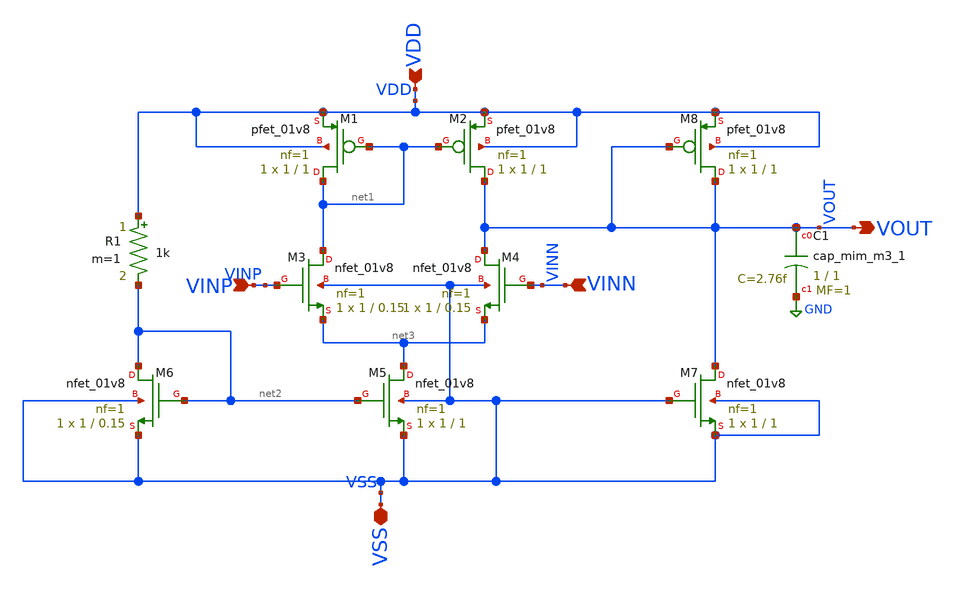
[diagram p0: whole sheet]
** sch_path: schematics/opamp_single_stage.sch
**.subckt opamp_single_stage VSS VOUT VDD VINP VINN
*.iopin VSS
*.opin VOUT
*.ipin VDD
*.ipin VINP
*.ipin VINN
XM1 net1 net1 VDD VDD sky130_fd_pr__pfet_01v8 L=1 W=1 nf=1 ad='int((nf+1)/2) * W/nf * 0.29' as='int((nf+2)/2) * W/nf * 0.29'
+ pd='2*int((nf+1)/2) * (W/nf + 0.29)' ps='2*int((nf+2)/2) * (W/nf + 0.29)' nrd='0.29 / W' nrs='0.29 / W'
+ sa=0 sb=0 sd=0 mult=1 m=1
XM2 VOUT net1 VDD VDD sky130_fd_pr__pfet_01v8 L=1 W=1 nf=1 ad='int((nf+1)/2) * W/nf * 0.29' as='int((nf+2)/2) * W/nf * 0.29'
+ pd='2*int((nf+1)/2) * (W/nf + 0.29)' ps='2*int((nf+2)/2) * (W/nf + 0.29)' nrd='0.29 / W' nrs='0.29 / W'
+ sa=0 sb=0 sd=0 mult=1 m=1
XM3 net1 VINP net3 VSS sky130_fd_pr__nfet_01v8 L=0.15 W=1 nf=1 ad='int((nf+1)/2) * W/nf * 0.29' as='int((nf+2)/2) * W/nf * 0.29'
+ pd='2*int((nf+1)/2) * (W/nf + 0.29)' ps='2*int((nf+2)/2) * (W/nf + 0.29)' nrd='0.29 / W' nrs='0.29 / W'
+ sa=0 sb=0 sd=0 mult=1 m=1
XM4 VOUT VINN net3 VSS sky130_fd_pr__nfet_01v8 L=0.15 W=1 nf=1 ad='int((nf+1)/2) * W/nf * 0.29' as='int((nf+2)/2) * W/nf * 0.29'
+ pd='2*int((nf+1)/2) * (W/nf + 0.29)' ps='2*int((nf+2)/2) * (W/nf + 0.29)' nrd='0.29 / W' nrs='0.29 / W'
+ sa=0 sb=0 sd=0 mult=1 m=1
XM5 net3 net2 VSS VSS sky130_fd_pr__nfet_01v8 L=1 W=1 nf=1 ad='int((nf+1)/2) * W/nf * 0.29' as='int((nf+2)/2) * W/nf * 0.29'
+ pd='2*int((nf+1)/2) * (W/nf + 0.29)' ps='2*int((nf+2)/2) * (W/nf + 0.29)' nrd='0.29 / W' nrs='0.29 / W'
+ sa=0 sb=0 sd=0 mult=1 m=1
XM6 net2 net2 VSS VSS sky130_fd_pr__nfet_01v8 L=0.15 W=1 nf=1 ad='int((nf+1)/2) * W/nf * 0.29' as='int((nf+2)/2) * W/nf * 0.29'
+ pd='2*int((nf+1)/2) * (W/nf + 0.29)' ps='2*int((nf+2)/2) * (W/nf + 0.29)' nrd='0.29 / W' nrs='0.29 / W'
+ sa=0 sb=0 sd=0 mult=1 m=1
XM7 VOUT VSS VSS VSS sky130_fd_pr__nfet_01v8 L=1 W=1 nf=1 ad='int((nf+1)/2) * W/nf * 0.29' as='int((nf+2)/2) * W/nf * 0.29'
+ pd='2*int((nf+1)/2) * (W/nf + 0.29)' ps='2*int((nf+2)/2) * (W/nf + 0.29)' nrd='0.29 / W' nrs='0.29 / W'
+ sa=0 sb=0 sd=0 mult=1 m=1
XM8 VOUT VOUT VDD VDD sky130_fd_pr__pfet_01v8 L=1 W=1 nf=1 ad='int((nf+1)/2) * W/nf * 0.29' as='int((nf+2)/2) * W/nf * 0.29'
+ pd='2*int((nf+1)/2) * (W/nf + 0.29)' ps='2*int((nf+2)/2) * (W/nf + 0.29)' nrd='0.29 / W' nrs='0.29 / W'
+ sa=0 sb=0 sd=0 mult=1 m=1
XC1 VOUT GND sky130_fd_pr__cap_mim_m3_1 W=1 L=1 MF=1 m=1
R1 VDD net2 1k m=1
**.ends
.GLOBAL GND
.end
